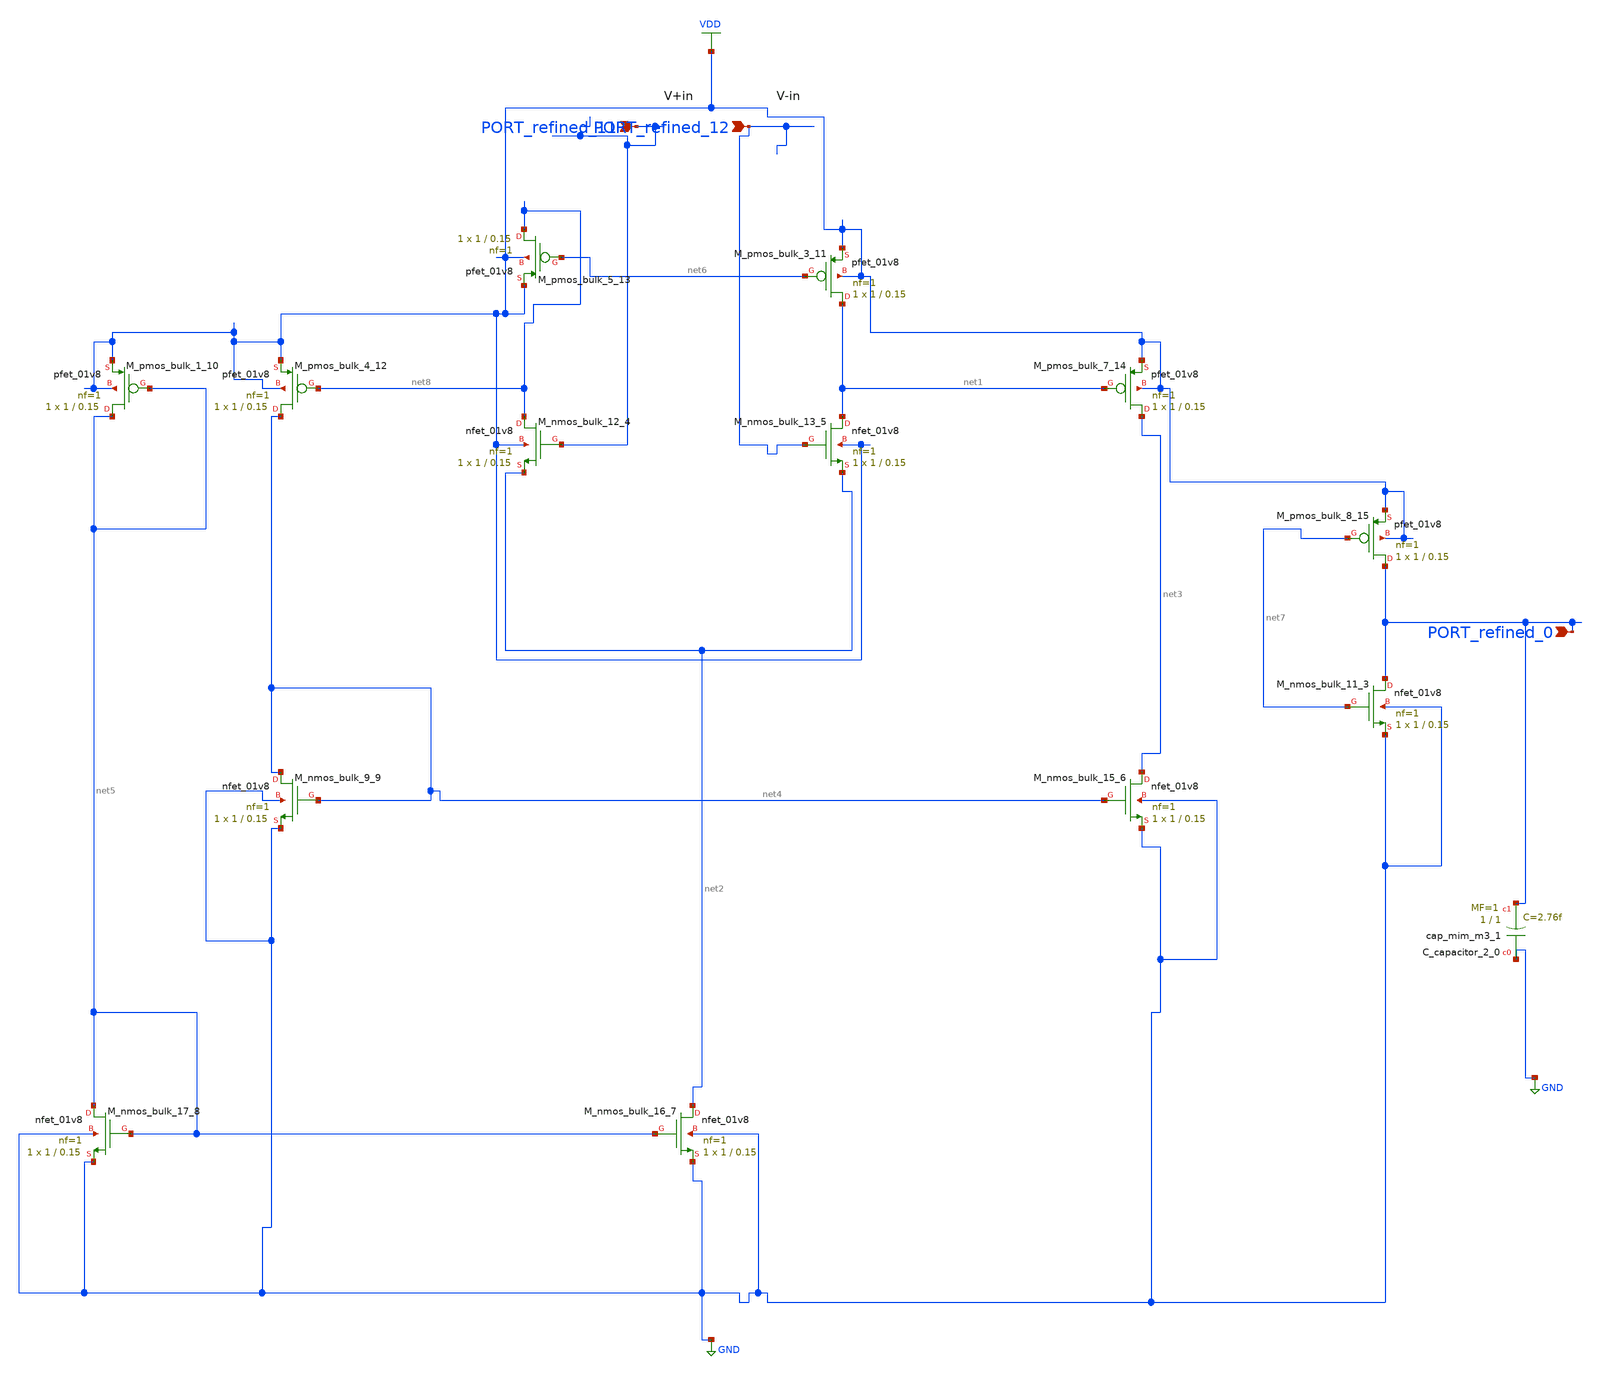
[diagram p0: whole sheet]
** sch_path: schematics/p05_fig2c.sch
**.subckt p05_fig2c PORT_refined_0 PORT_refined_11 PORT_refined_12
*.ipin PORT_refined_0
*.ipin PORT_refined_11
*.ipin PORT_refined_12
XC_capacitor_2_0 GND PORT_refined_0 sky130_fd_pr__cap_mim_m3_1 W=1 L=1 MF=1 m=1
XM_nmos_bulk_11_3 PORT_refined_0 net7 GND GND sky130_fd_pr__nfet_01v8 L=0.15 W=1 nf=1 ad='int((1 + 1)/2) * 1 / 1 * 0.29'
+ as='int((1 + 2)/2) * 1 / 1 * 0.29' pd='2*int((1 + 1)/2) * (1 / 1 + 0.29)' ps='2*int((1 + 2)/2) * (1 / 1 + 0.29)'
+ nrd='0.29 / 1 ' nrs='0.29 / 1 ' sa=0 sb=0 sd=0 mult=1 m=1
XM_nmos_bulk_12_4 net8 PORT_refined_11 net2 VDD sky130_fd_pr__nfet_01v8 L=0.15 W=1 nf=1 ad='int((1 + 1)/2) * 1 / 1 * 0.29'
+ as='int((1 + 2)/2) * 1 / 1 * 0.29' pd='2*int((1 + 1)/2) * (1 / 1 + 0.29)' ps='2*int((1 + 2)/2) * (1 / 1 + 0.29)'
+ nrd='0.29 / 1 ' nrs='0.29 / 1 ' sa=0 sb=0 sd=0 mult=1 m=1
XM_nmos_bulk_13_5 net1 PORT_refined_12 net2 VDD sky130_fd_pr__nfet_01v8 L=0.15 W=1 nf=1 ad='int((1 + 1)/2) * 1 / 1 * 0.29'
+ as='int((1 + 2)/2) * 1 / 1 * 0.29' pd='2*int((1 + 1)/2) * (1 / 1 + 0.29)' ps='2*int((1 + 2)/2) * (1 / 1 + 0.29)'
+ nrd='0.29 / 1 ' nrs='0.29 / 1 ' sa=0 sb=0 sd=0 mult=1 m=1
XM_nmos_bulk_15_6 net3 net4 GND GND sky130_fd_pr__nfet_01v8 L=0.15 W=1 nf=1 ad='int((1 + 1)/2) * 1 / 1 * 0.29'
+ as='int((1 + 2)/2) * 1 / 1 * 0.29' pd='2*int((1 + 1)/2) * (1 / 1 + 0.29)' ps='2*int((1 + 2)/2) * (1 / 1 + 0.29)'
+ nrd='0.29 / 1 ' nrs='0.29 / 1 ' sa=0 sb=0 sd=0 mult=1 m=1
XM_nmos_bulk_16_7 net2 net5 GND GND sky130_fd_pr__nfet_01v8 L=0.15 W=1 nf=1 ad='int((1 + 1)/2) * 1 / 1 * 0.29'
+ as='int((1 + 2)/2) * 1 / 1 * 0.29' pd='2*int((1 + 1)/2) * (1 / 1 + 0.29)' ps='2*int((1 + 2)/2) * (1 / 1 + 0.29)'
+ nrd='0.29 / 1 ' nrs='0.29 / 1 ' sa=0 sb=0 sd=0 mult=1 m=1
XM_nmos_bulk_17_8 net5 net5 GND GND sky130_fd_pr__nfet_01v8 L=0.15 W=1 nf=1 ad='int((1 + 1)/2) * 1 / 1 * 0.29'
+ as='int((1 + 2)/2) * 1 / 1 * 0.29' pd='2*int((1 + 1)/2) * (1 / 1 + 0.29)' ps='2*int((1 + 2)/2) * (1 / 1 + 0.29)'
+ nrd='0.29 / 1 ' nrs='0.29 / 1 ' sa=0 sb=0 sd=0 mult=1 m=1
XM_nmos_bulk_9_9 net4 net4 GND GND sky130_fd_pr__nfet_01v8 L=0.15 W=1 nf=1 ad='int((1 + 1)/2) * 1 / 1 * 0.29'
+ as='int((1 + 2)/2) * 1 / 1 * 0.29' pd='2*int((1 + 1)/2) * (1 / 1 + 0.29)' ps='2*int((1 + 2)/2) * (1 / 1 + 0.29)'
+ nrd='0.29 / 1 ' nrs='0.29 / 1 ' sa=0 sb=0 sd=0 mult=1 m=1
XM_pmos_bulk_1_10 net5 net5 VDD VDD sky130_fd_pr__pfet_01v8 L=0.15 W=1 nf=1 ad='int((1 + 1)/2) * 1 / 1 * 0.29'
+ as='int((1 + 2)/2) * 1 / 1 * 0.29' pd='2*int((1 + 1)/2) * (1 / 1 + 0.29)' ps='2*int((1 + 2)/2) * (1 / 1 + 0.29)'
+ nrd='0.29 / 1 ' nrs='0.29 / 1 ' sa=0 sb=0 sd=0 mult=1 m=1
XM_pmos_bulk_3_11 net1 net6 VDD VDD sky130_fd_pr__pfet_01v8 L=0.15 W=1 nf=1 ad='int((1 + 1)/2) * 1 / 1 * 0.29'
+ as='int((1 + 2)/2) * 1 / 1 * 0.29' pd='2*int((1 + 1)/2) * (1 / 1 + 0.29)' ps='2*int((1 + 2)/2) * (1 / 1 + 0.29)'
+ nrd='0.29 / 1 ' nrs='0.29 / 1 ' sa=0 sb=0 sd=0 mult=1 m=1
XM_pmos_bulk_4_12 net4 net8 VDD VDD sky130_fd_pr__pfet_01v8 L=0.15 W=1 nf=1 ad='int((1 + 1)/2) * 1 / 1 * 0.29'
+ as='int((1 + 2)/2) * 1 / 1 * 0.29' pd='2*int((1 + 1)/2) * (1 / 1 + 0.29)' ps='2*int((1 + 2)/2) * (1 / 1 + 0.29)'
+ nrd='0.29 / 1 ' nrs='0.29 / 1 ' sa=0 sb=0 sd=0 mult=1 m=1
XM_pmos_bulk_5_13 net8 net6 VDD VDD sky130_fd_pr__pfet_01v8 L=0.15 W=1 nf=1 ad='int((1 + 1)/2) * 1 / 1 * 0.29'
+ as='int((1 + 2)/2) * 1 / 1 * 0.29' pd='2*int((1 + 1)/2) * (1 / 1 + 0.29)' ps='2*int((1 + 2)/2) * (1 / 1 + 0.29)'
+ nrd='0.29 / 1 ' nrs='0.29 / 1 ' sa=0 sb=0 sd=0 mult=1 m=1
XM_pmos_bulk_7_14 net3 net1 VDD VDD sky130_fd_pr__pfet_01v8 L=0.15 W=1 nf=1 ad='int((1 + 1)/2) * 1 / 1 * 0.29'
+ as='int((1 + 2)/2) * 1 / 1 * 0.29' pd='2*int((1 + 1)/2) * (1 / 1 + 0.29)' ps='2*int((1 + 2)/2) * (1 / 1 + 0.29)'
+ nrd='0.29 / 1 ' nrs='0.29 / 1 ' sa=0 sb=0 sd=0 mult=1 m=1
XM_pmos_bulk_8_15 PORT_refined_0 net7 VDD VDD sky130_fd_pr__pfet_01v8 L=0.15 W=1 nf=1 ad='int((1 + 1)/2) * 1 / 1 * 0.29'
+ as='int((1 + 2)/2) * 1 / 1 * 0.29' pd='2*int((1 + 1)/2) * (1 / 1 + 0.29)' ps='2*int((1 + 2)/2) * (1 / 1 + 0.29)'
+ nrd='0.29 / 1 ' nrs='0.29 / 1 ' sa=0 sb=0 sd=0 mult=1 m=1
**.ends
.GLOBAL GND
.GLOBAL VDD
.end
